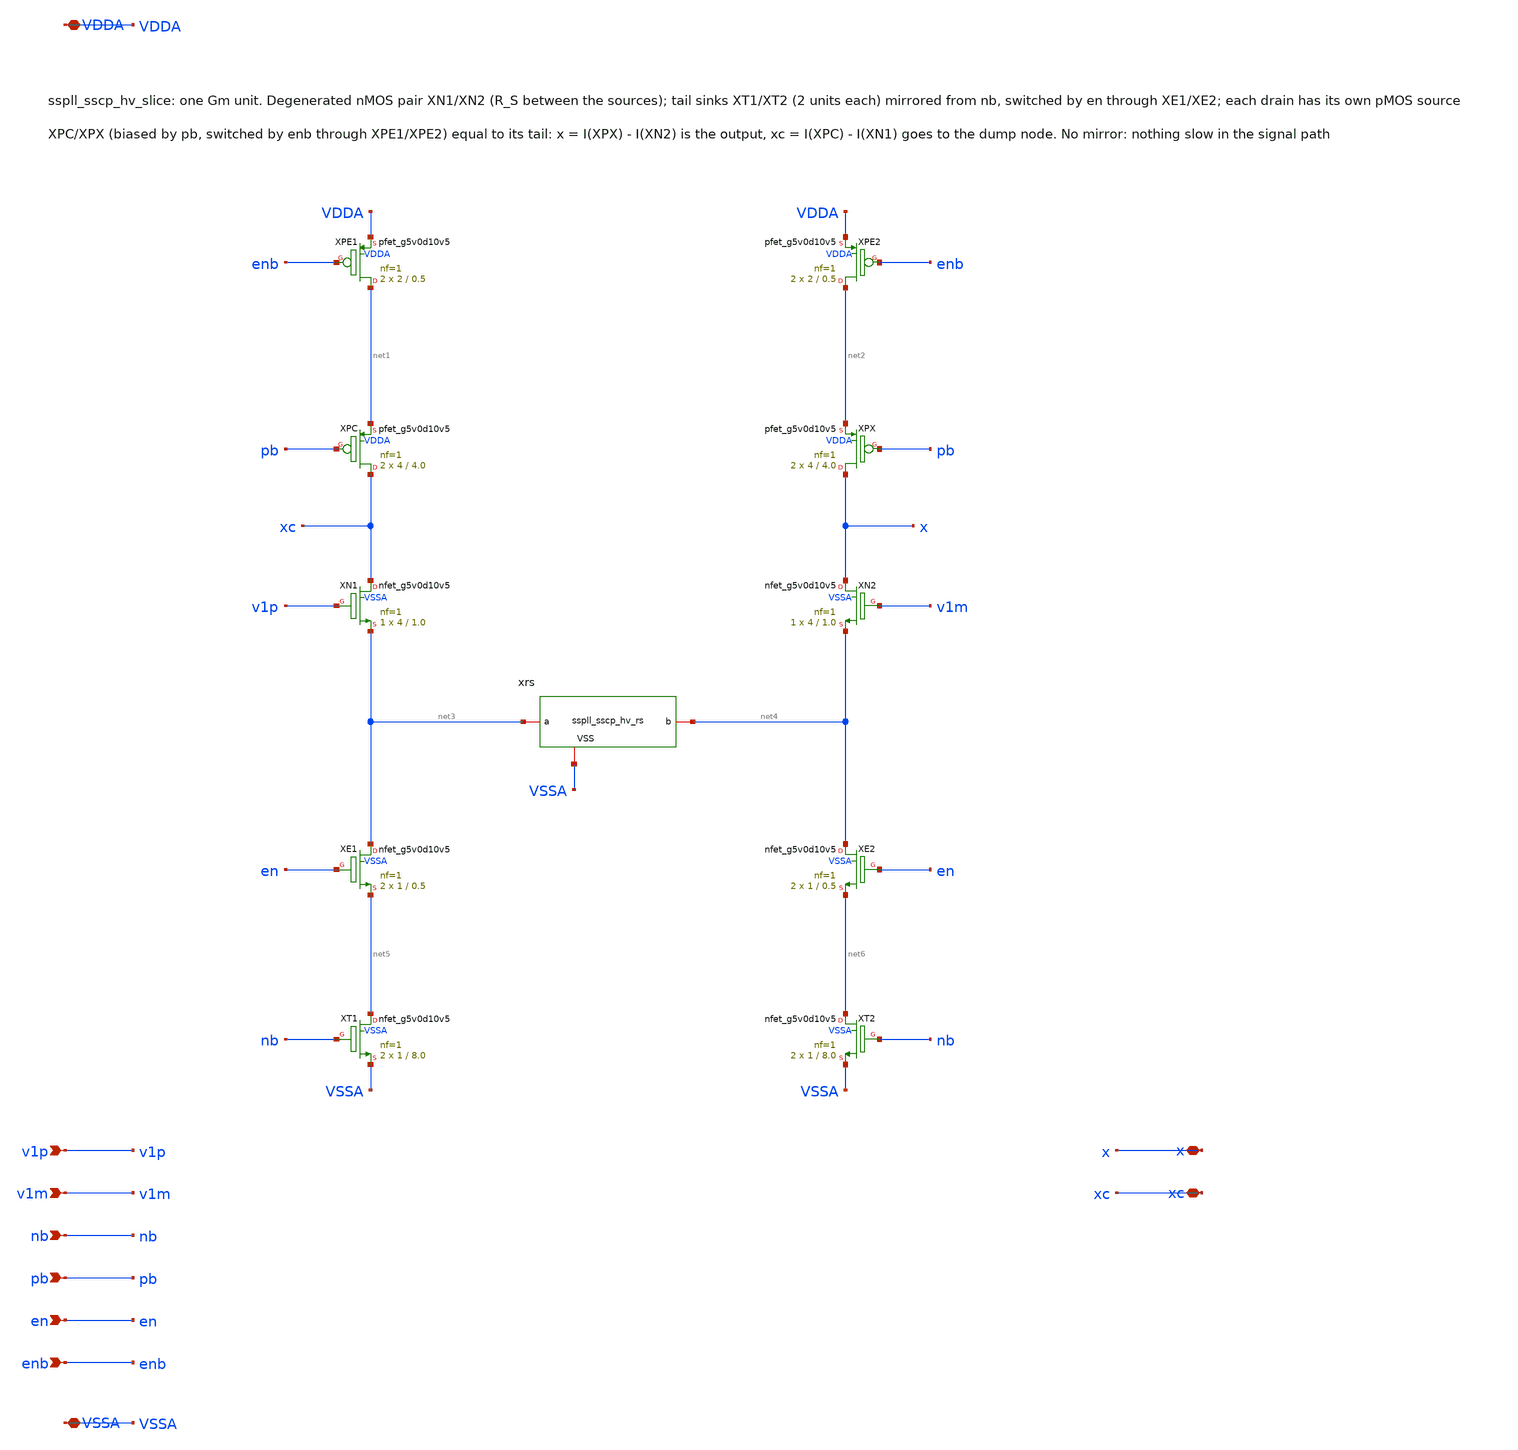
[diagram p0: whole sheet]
** sch_path: xschem/sscp_hv/sspll_sscp_hv_slice.sch
**.subckt sspll_sscp_hv_slice v1p v1m nb pb en enb x xc VDDA VSSA
*.ipin v1p
*.ipin v1m
*.ipin nb
*.ipin pb
*.ipin en
*.ipin enb
*.iopin x
*.iopin xc
*.iopin VDDA
*.iopin VSSA
XXPE1 net1 enb VDDA VDDA sky130_fd_pr__pfet_g5v0d10v5 L=0.5 W=2 nf=1 ad='int((nf+1)/2) * W/nf * 0.29'
+ as='int((nf+2)/2) * W/nf * 0.29' pd='2*int((nf+1)/2) * (W/nf + 0.29)' ps='2*int((nf+2)/2) * (W/nf + 0.29)'
+ nrd='0.29 / W' nrs='0.29 / W' sa=0 sb=0 sd=0 mult=2 m=2
XXPE2 net2 enb VDDA VDDA sky130_fd_pr__pfet_g5v0d10v5 L=0.5 W=2 nf=1 ad='int((nf+1)/2) * W/nf * 0.29'
+ as='int((nf+2)/2) * W/nf * 0.29' pd='2*int((nf+1)/2) * (W/nf + 0.29)' ps='2*int((nf+2)/2) * (W/nf + 0.29)'
+ nrd='0.29 / W' nrs='0.29 / W' sa=0 sb=0 sd=0 mult=2 m=2
XXPC xc pb net1 VDDA sky130_fd_pr__pfet_g5v0d10v5 L=4.0 W=4 nf=1 ad='int((nf+1)/2) * W/nf * 0.29' as='int((nf+2)/2) * W/nf * 0.29'
+ pd='2*int((nf+1)/2) * (W/nf + 0.29)' ps='2*int((nf+2)/2) * (W/nf + 0.29)' nrd='0.29 / W' nrs='0.29 / W'
+ sa=0 sb=0 sd=0 mult=2 m=2
XXPX x pb net2 VDDA sky130_fd_pr__pfet_g5v0d10v5 L=4.0 W=4 nf=1 ad='int((nf+1)/2) * W/nf * 0.29' as='int((nf+2)/2) * W/nf * 0.29'
+ pd='2*int((nf+1)/2) * (W/nf + 0.29)' ps='2*int((nf+2)/2) * (W/nf + 0.29)' nrd='0.29 / W' nrs='0.29 / W'
+ sa=0 sb=0 sd=0 mult=2 m=2
XXN1 xc v1p net3 VSSA sky130_fd_pr__nfet_g5v0d10v5 L=1.0 W=4 nf=1 ad='int((nf+1)/2) * W/nf * 0.29' as='int((nf+2)/2) * W/nf * 0.29'
+ pd='2*int((nf+1)/2) * (W/nf + 0.29)' ps='2*int((nf+2)/2) * (W/nf + 0.29)' nrd='0.29 / W' nrs='0.29 / W'
+ sa=0 sb=0 sd=0 mult=1 m=1
XXN2 x v1m net4 VSSA sky130_fd_pr__nfet_g5v0d10v5 L=1.0 W=4 nf=1 ad='int((nf+1)/2) * W/nf * 0.29' as='int((nf+2)/2) * W/nf * 0.29'
+ pd='2*int((nf+1)/2) * (W/nf + 0.29)' ps='2*int((nf+2)/2) * (W/nf + 0.29)' nrd='0.29 / W' nrs='0.29 / W'
+ sa=0 sb=0 sd=0 mult=1 m=1
xrs net3 net4 VSSA sspll_sscp_hv_rs
XXE1 net3 en net5 VSSA sky130_fd_pr__nfet_g5v0d10v5 L=0.5 W=1 nf=1 ad='int((nf+1)/2) * W/nf * 0.29' as='int((nf+2)/2) * W/nf * 0.29'
+ pd='2*int((nf+1)/2) * (W/nf + 0.29)' ps='2*int((nf+2)/2) * (W/nf + 0.29)' nrd='0.29 / W' nrs='0.29 / W'
+ sa=0 sb=0 sd=0 mult=2 m=2
XXE2 net4 en net6 VSSA sky130_fd_pr__nfet_g5v0d10v5 L=0.5 W=1 nf=1 ad='int((nf+1)/2) * W/nf * 0.29' as='int((nf+2)/2) * W/nf * 0.29'
+ pd='2*int((nf+1)/2) * (W/nf + 0.29)' ps='2*int((nf+2)/2) * (W/nf + 0.29)' nrd='0.29 / W' nrs='0.29 / W'
+ sa=0 sb=0 sd=0 mult=2 m=2
XXT1 net5 nb VSSA VSSA sky130_fd_pr__nfet_g5v0d10v5 L=8.0 W=1 nf=1 ad='int((nf+1)/2) * W/nf * 0.29' as='int((nf+2)/2) * W/nf * 0.29'
+ pd='2*int((nf+1)/2) * (W/nf + 0.29)' ps='2*int((nf+2)/2) * (W/nf + 0.29)' nrd='0.29 / W' nrs='0.29 / W'
+ sa=0 sb=0 sd=0 mult=2 m=2
XXT2 net6 nb VSSA VSSA sky130_fd_pr__nfet_g5v0d10v5 L=8.0 W=1 nf=1 ad='int((nf+1)/2) * W/nf * 0.29' as='int((nf+2)/2) * W/nf * 0.29'
+ pd='2*int((nf+1)/2) * (W/nf + 0.29)' ps='2*int((nf+2)/2) * (W/nf + 0.29)' nrd='0.29 / W' nrs='0.29 / W'
+ sa=0 sb=0 sd=0 mult=2 m=2
**.ends

* expanding   symbol:  sspll_sscp_hv_rs.sym # of pins=3
** sym_path: xschem/sscp_hv/sspll_sscp_hv_rs.sym
** sch_path: xschem/sscp_hv/sspll_sscp_hv_rs.sch
.subckt sspll_sscp_hv_rs a b VSS
*.iopin a
*.iopin b
*.iopin VSS
XXR0 b a VSS sky130_fd_pr__res_xhigh_po_0p35 L=17.2 mult=1 m=1
.ends

.end
